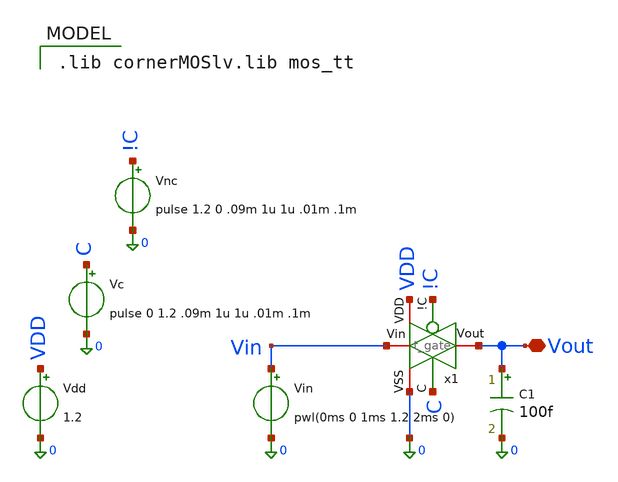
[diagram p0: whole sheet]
** sch_path: xschem/t_gate_tb.sch
**.subckt t_gate_tb Vout
*.iopin Vout
Vin Vin 0 pwl(0ms 0 1ms 1.2 2ms 0)
Vdd VDD 0 1.2
C1 Vout 0 100f m=1
x1 !C VDD Vout Vin 0 C t_gate
Vc C 0 pulse 0 1.2 .09m 1u 1u .01m .1m
Vnc !C 0 pulse 1.2 0 .09m 1u 1u .01m .1m
**** begin user architecture code
 .lib cornerMOSlv.lib mos_tt



.param temp=27
.control
op
write t_gate_tb.raw
set appendwrite
reset
save all
tran 1us 2ms
write t_gate_tb.raw
quit 0
.endc


**** end user architecture code
**.ends

* expanding   symbol:  t_gate.sym # of pins=6
** sym_path: xschem/t_gate.sym
** sch_path: xschem/t_gate.sch
.subckt t_gate !C VDD Vout Vin VSS C
*.iopin VSS
*.iopin VDD
*.iopin Vout
*.iopin Vin
*.ipin C
*.ipin !C
XM1 Vin C Vout VSS sg13_lv_nmos w=0.15u l=0.13u ng=1 m=1 mm_ok=1
XM2 Vin !C Vout VDD sg13_lv_pmos w=0.3u l=0.13u ng=1 m=1 mm_ok=1
.ends

.end
